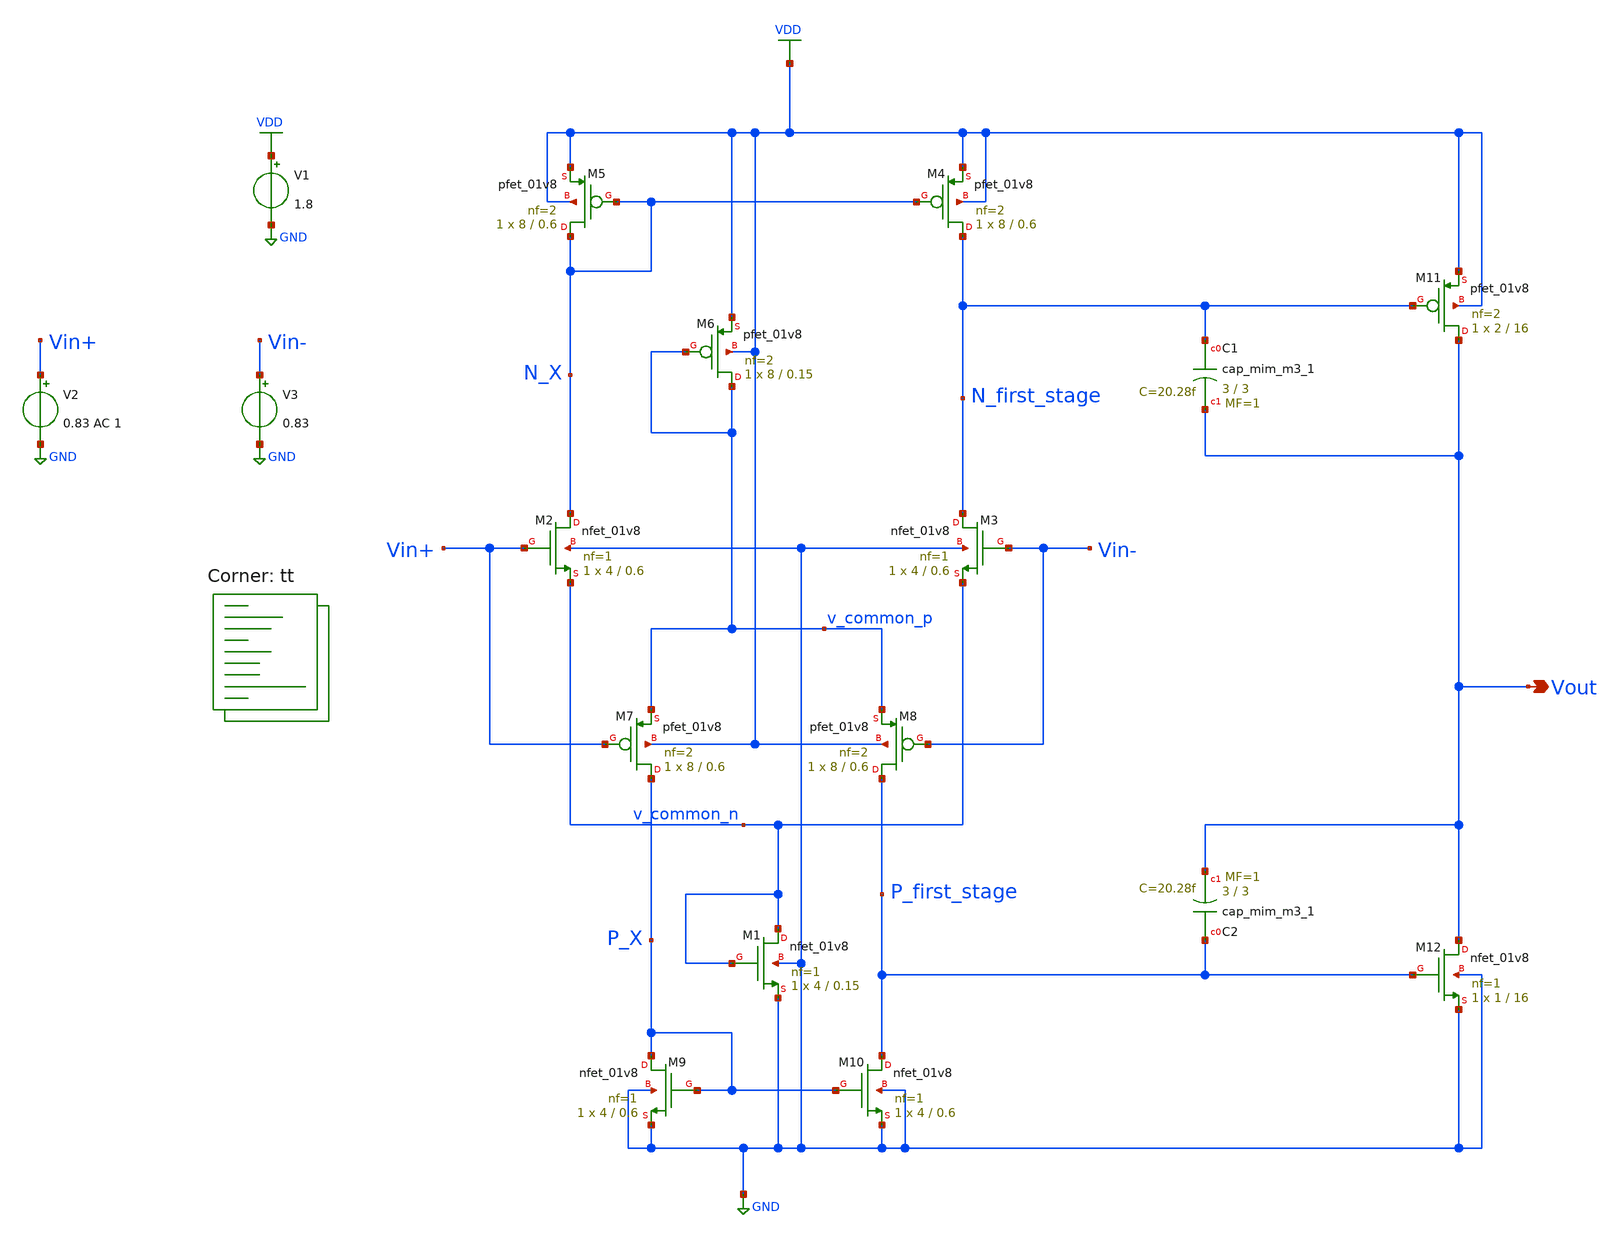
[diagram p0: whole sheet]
** sch_path: projects/pll/charge_pump/xschem_ngspice/tb_rail_to_rail_opamp7.sch
**.subckt tb_rail_to_rail_opamp7 Vout
*.opin Vout
V1 VDD GND 1.8
V2 Vin+ GND 0.83 AC 1
V3 Vin- GND 0.83
XM2 N_X Vin+ v_common_n GND sky130_fd_pr__nfet_01v8 L=0.6 W=4 nf=1 ad='int((nf+1)/2) * W/nf * 0.29' as='int((nf+2)/2) * W/nf * 0.29'
+ pd='2*int((nf+1)/2) * (W/nf + 0.29)' ps='2*int((nf+2)/2) * (W/nf + 0.29)' nrd='0.29 / W' nrs='0.29 / W'
+ sa=0 sb=0 sd=0 mult=1 m=1
XM3 N_first_stage Vin- v_common_n GND sky130_fd_pr__nfet_01v8 L=0.6 W=4 nf=1 ad='int((nf+1)/2) * W/nf * 0.29'
+ as='int((nf+2)/2) * W/nf * 0.29' pd='2*int((nf+1)/2) * (W/nf + 0.29)' ps='2*int((nf+2)/2) * (W/nf + 0.29)'
+ nrd='0.29 / W' nrs='0.29 / W' sa=0 sb=0 sd=0 mult=1 m=1
XM5 N_X N_X VDD VDD sky130_fd_pr__pfet_01v8 L=0.6 W=8 nf=2 ad='int((nf+1)/2) * W/nf * 0.29' as='int((nf+2)/2) * W/nf * 0.29'
+ pd='2*int((nf+1)/2) * (W/nf + 0.29)' ps='2*int((nf+2)/2) * (W/nf + 0.29)' nrd='0.29 / W' nrs='0.29 / W'
+ sa=0 sb=0 sd=0 mult=1 m=1
XM4 N_first_stage N_X VDD VDD sky130_fd_pr__pfet_01v8 L=0.6 W=8 nf=2 ad='int((nf+1)/2) * W/nf * 0.29'
+ as='int((nf+2)/2) * W/nf * 0.29' pd='2*int((nf+1)/2) * (W/nf + 0.29)' ps='2*int((nf+2)/2) * (W/nf + 0.29)'
+ nrd='0.29 / W' nrs='0.29 / W' sa=0 sb=0 sd=0 mult=1 m=1
XM6 v_common_p v_common_p VDD VDD sky130_fd_pr__pfet_01v8 L=0.15 W=8 nf=2 ad='int((nf+1)/2) * W/nf * 0.29'
+ as='int((nf+2)/2) * W/nf * 0.29' pd='2*int((nf+1)/2) * (W/nf + 0.29)' ps='2*int((nf+2)/2) * (W/nf + 0.29)'
+ nrd='0.29 / W' nrs='0.29 / W' sa=0 sb=0 sd=0 mult=1 m=1
XM7 P_X Vin+ v_common_p VDD sky130_fd_pr__pfet_01v8 L=0.6 W=8 nf=2 ad='int((nf+1)/2) * W/nf * 0.29' as='int((nf+2)/2) * W/nf * 0.29'
+ pd='2*int((nf+1)/2) * (W/nf + 0.29)' ps='2*int((nf+2)/2) * (W/nf + 0.29)' nrd='0.29 / W' nrs='0.29 / W'
+ sa=0 sb=0 sd=0 mult=1 m=1
XM8 P_first_stage Vin- v_common_p VDD sky130_fd_pr__pfet_01v8 L=0.6 W=8 nf=2 ad='int((nf+1)/2) * W/nf * 0.29'
+ as='int((nf+2)/2) * W/nf * 0.29' pd='2*int((nf+1)/2) * (W/nf + 0.29)' ps='2*int((nf+2)/2) * (W/nf + 0.29)'
+ nrd='0.29 / W' nrs='0.29 / W' sa=0 sb=0 sd=0 mult=1 m=1
XM9 P_X P_X GND GND sky130_fd_pr__nfet_01v8 L=0.6 W=4 nf=1 ad='int((nf+1)/2) * W/nf * 0.29' as='int((nf+2)/2) * W/nf * 0.29'
+ pd='2*int((nf+1)/2) * (W/nf + 0.29)' ps='2*int((nf+2)/2) * (W/nf + 0.29)' nrd='0.29 / W' nrs='0.29 / W'
+ sa=0 sb=0 sd=0 mult=1 m=1
XM10 P_first_stage P_X GND GND sky130_fd_pr__nfet_01v8 L=0.6 W=4 nf=1 ad='int((nf+1)/2) * W/nf * 0.29'
+ as='int((nf+2)/2) * W/nf * 0.29' pd='2*int((nf+1)/2) * (W/nf + 0.29)' ps='2*int((nf+2)/2) * (W/nf + 0.29)'
+ nrd='0.29 / W' nrs='0.29 / W' sa=0 sb=0 sd=0 mult=1 m=1
XM1 v_common_n v_common_n GND GND sky130_fd_pr__nfet_01v8 L=0.15 W=4 nf=1 ad='int((nf+1)/2) * W/nf * 0.29'
+ as='int((nf+2)/2) * W/nf * 0.29' pd='2*int((nf+1)/2) * (W/nf + 0.29)' ps='2*int((nf+2)/2) * (W/nf + 0.29)'
+ nrd='0.29 / W' nrs='0.29 / W' sa=0 sb=0 sd=0 mult=1 m=1
XM11 Vout N_first_stage VDD VDD sky130_fd_pr__pfet_01v8 L=16 W=2 nf=2 ad='int((nf+1)/2) * W/nf * 0.29'
+ as='int((nf+2)/2) * W/nf * 0.29' pd='2*int((nf+1)/2) * (W/nf + 0.29)' ps='2*int((nf+2)/2) * (W/nf + 0.29)'
+ nrd='0.29 / W' nrs='0.29 / W' sa=0 sb=0 sd=0 mult=1 m=1
XM12 Vout P_first_stage GND GND sky130_fd_pr__nfet_01v8 L=16 W=1 nf=1 ad='int((nf+1)/2) * W/nf * 0.29'
+ as='int((nf+2)/2) * W/nf * 0.29' pd='2*int((nf+1)/2) * (W/nf + 0.29)' ps='2*int((nf+2)/2) * (W/nf + 0.29)'
+ nrd='0.29 / W' nrs='0.29 / W' sa=0 sb=0 sd=0 mult=1 m=1
XC1 N_first_stage Vout sky130_fd_pr__cap_mim_m3_1 W=3 L=3 MF=1 m=1
XC2 P_first_stage Vout sky130_fd_pr__cap_mim_m3_1 W=3 L=3 MF=1 m=1
**** begin user architecture code



.option wnflag=1
.option savecurrents


.save @m.xm1.msky130_fd_pr__nfet_01v8[gm] @m.xm2.msky130_fd_pr__nfet_01v8[gm] @m.xm3.msky130_fd_pr__nfet_01v8[gm] @m.xm4.msky130_fd_pr__pfet_01v8[gm] @m.xm5.msky130_fd_pr__pfet_01v8[gm] @m.xm6.msky130_fd_pr__pfet_01v8[gm] @m.xm7.msky130_fd_pr__pfet_01v8[gm] @m.xm8.msky130_fd_pr__pfet_01v8[gm] @m.xm9.msky130_fd_pr__nfet_01v8[gm] @m.xm10.msky130_fd_pr__nfet_01v8[gm] @m.xm11.msky130_fd_pr__pfet_01v8[gm] @m.xm12.msky130_fd_pr__nfet_01v8[gm] @m.xm13.msky130_fd_pr__nfet_01v8[gm] @m.xm14.msky130_fd_pr__nfet_01v8[gm] @m.xm15.msky130_fd_pr__pfet_01v8[gm]


.control
  save all
  ac dec 20 1 1T
  * tran 50p 2u
  * dc V2 0 1.8 0.01
  write tb_rail_to_rail_opamp7.raw
  set appendwrite
.endc



.lib $::SKYWATER_MODELS/sky130.lib.spice tt
**** end user architecture code
**.ends
.GLOBAL GND
.GLOBAL VDD
.end
